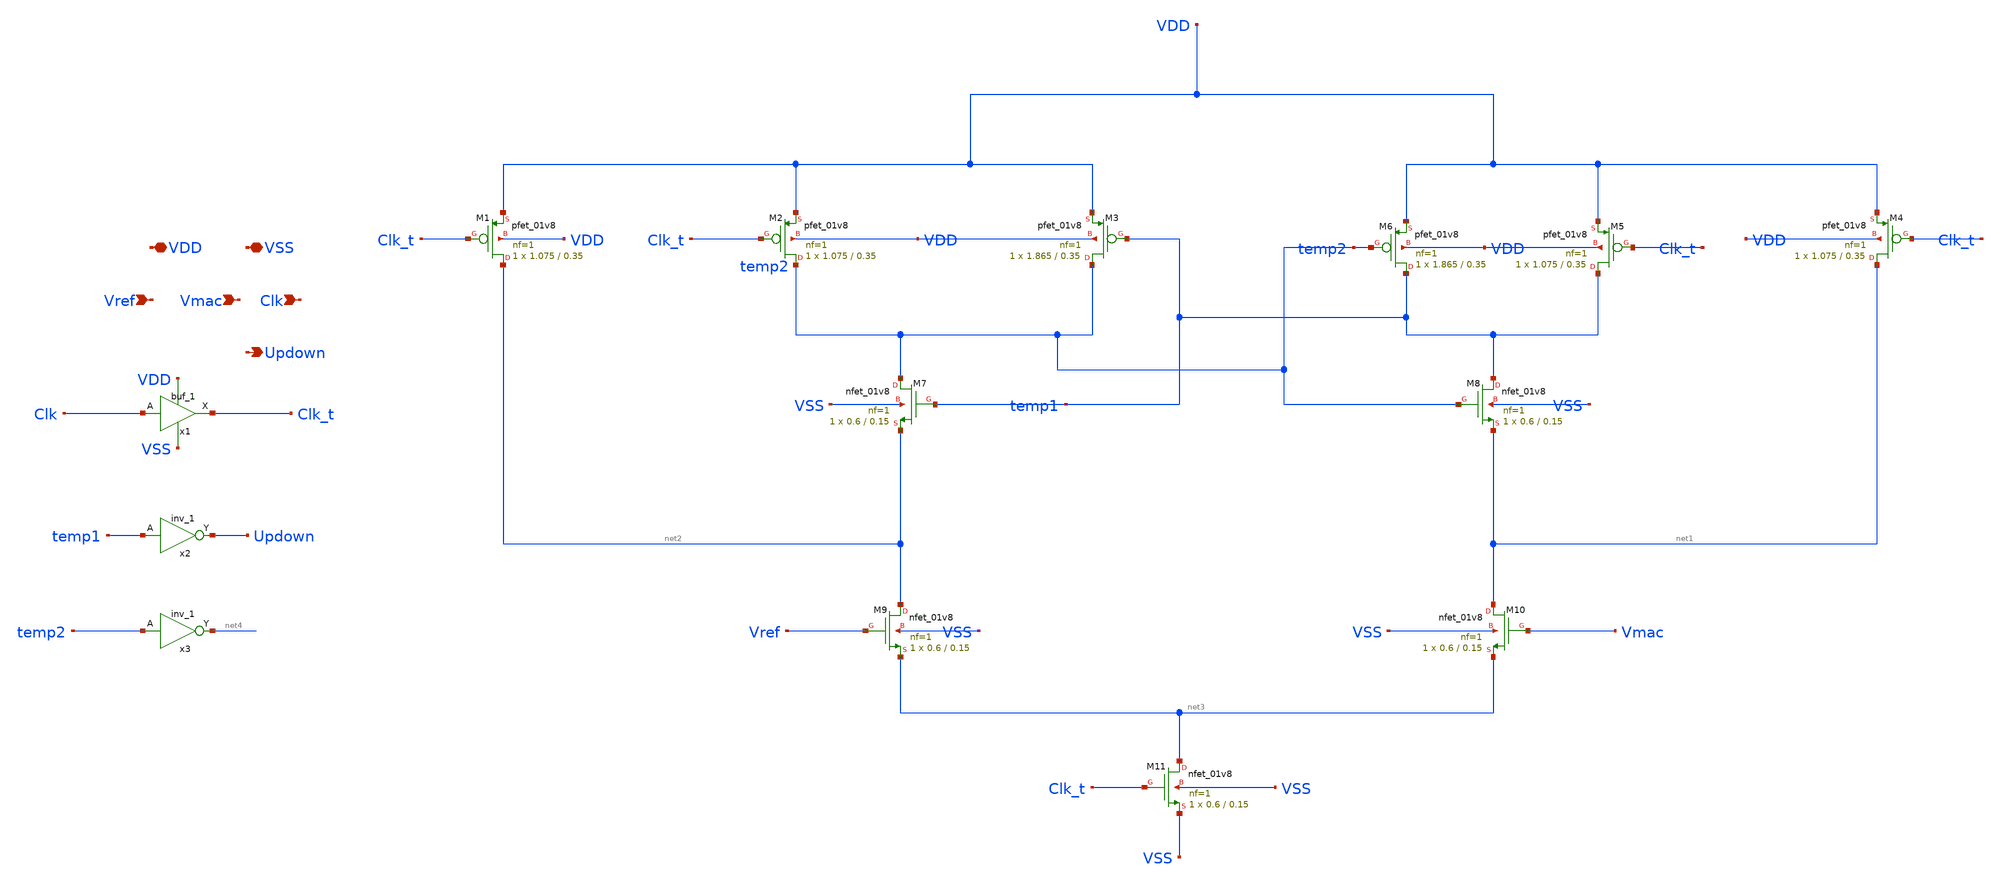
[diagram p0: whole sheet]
** sch_path: adc_comp/adc_8bit.sch
**.subckt adc_8bit VSS VDD Vref Vmac Clk Updown
*.iopin VSS
*.iopin VDD
*.ipin Vref
*.ipin Vmac
*.ipin Clk
*.opin Updown
x1 Clk VSS VNB VPB VDD Clk_t sky130_fd_sc_hd__buf_1
x2 temp1 VSS VNB VPB VDD Updown sky130_fd_sc_hd__inv_1
x3 temp2 VSS VNB VPB VDD net4 sky130_fd_sc_hd__inv_1
XM1 net2 Clk_t VDD VDD sky130_fd_pr__pfet_01v8 L=0.35 W=1.075 nf=1 ad='int((nf+1)/2) * W/nf * 0.29' as='int((nf+2)/2) * W/nf * 0.29'
+ pd='2*int((nf+1)/2) * (W/nf + 0.29)' ps='2*int((nf+2)/2) * (W/nf + 0.29)' nrd='0.29 / W' nrs='0.29 / W'
+ sa=0 sb=0 sd=0 mult=1 m=1
XM2 temp2 Clk_t VDD VDD sky130_fd_pr__pfet_01v8 L=0.35 W=1.075 nf=1 ad='int((nf+1)/2) * W/nf * 0.29'
+ as='int((nf+2)/2) * W/nf * 0.29' pd='2*int((nf+1)/2) * (W/nf + 0.29)' ps='2*int((nf+2)/2) * (W/nf + 0.29)'
+ nrd='0.29 / W' nrs='0.29 / W' sa=0 sb=0 sd=0 mult=1 m=1
XM3 temp2 temp1 VDD VDD sky130_fd_pr__pfet_01v8 L=0.35 W=1.865 nf=1 ad='int((nf+1)/2) * W/nf * 0.29'
+ as='int((nf+2)/2) * W/nf * 0.29' pd='2*int((nf+1)/2) * (W/nf + 0.29)' ps='2*int((nf+2)/2) * (W/nf + 0.29)'
+ nrd='0.29 / W' nrs='0.29 / W' sa=0 sb=0 sd=0 mult=1 m=1
XM4 net1 Clk_t VDD VDD sky130_fd_pr__pfet_01v8 L=0.35 W=1.075 nf=1 ad='int((nf+1)/2) * W/nf * 0.29' as='int((nf+2)/2) * W/nf * 0.29'
+ pd='2*int((nf+1)/2) * (W/nf + 0.29)' ps='2*int((nf+2)/2) * (W/nf + 0.29)' nrd='0.29 / W' nrs='0.29 / W'
+ sa=0 sb=0 sd=0 mult=1 m=1
XM5 temp1 Clk_t VDD VDD sky130_fd_pr__pfet_01v8 L=0.35 W=1.075 nf=1 ad='int((nf+1)/2) * W/nf * 0.29'
+ as='int((nf+2)/2) * W/nf * 0.29' pd='2*int((nf+1)/2) * (W/nf + 0.29)' ps='2*int((nf+2)/2) * (W/nf + 0.29)'
+ nrd='0.29 / W' nrs='0.29 / W' sa=0 sb=0 sd=0 mult=1 m=1
XM6 temp1 temp2 VDD VDD sky130_fd_pr__pfet_01v8 L=0.35 W=1.865 nf=1 ad='int((nf+1)/2) * W/nf * 0.29'
+ as='int((nf+2)/2) * W/nf * 0.29' pd='2*int((nf+1)/2) * (W/nf + 0.29)' ps='2*int((nf+2)/2) * (W/nf + 0.29)'
+ nrd='0.29 / W' nrs='0.29 / W' sa=0 sb=0 sd=0 mult=1 m=1
XM7 temp2 temp1 net2 VSS sky130_fd_pr__nfet_01v8 L=0.15 W=0.6 nf=1 ad='int((nf+1)/2) * W/nf * 0.29' as='int((nf+2)/2) * W/nf * 0.29'
+ pd='2*int((nf+1)/2) * (W/nf + 0.29)' ps='2*int((nf+2)/2) * (W/nf + 0.29)' nrd='0.29 / W' nrs='0.29 / W'
+ sa=0 sb=0 sd=0 mult=1 m=1
XM8 temp1 temp2 net1 VSS sky130_fd_pr__nfet_01v8 L=0.15 W=0.6 nf=1 ad='int((nf+1)/2) * W/nf * 0.29' as='int((nf+2)/2) * W/nf * 0.29'
+ pd='2*int((nf+1)/2) * (W/nf + 0.29)' ps='2*int((nf+2)/2) * (W/nf + 0.29)' nrd='0.29 / W' nrs='0.29 / W'
+ sa=0 sb=0 sd=0 mult=1 m=1
XM9 net2 Vref net3 VSS sky130_fd_pr__nfet_01v8 L=0.15 W=0.6 nf=1 ad='int((nf+1)/2) * W/nf * 0.29' as='int((nf+2)/2) * W/nf * 0.29'
+ pd='2*int((nf+1)/2) * (W/nf + 0.29)' ps='2*int((nf+2)/2) * (W/nf + 0.29)' nrd='0.29 / W' nrs='0.29 / W'
+ sa=0 sb=0 sd=0 mult=1 m=1
XM10 net1 Vmac net3 VSS sky130_fd_pr__nfet_01v8 L=0.15 W=0.6 nf=1 ad='int((nf+1)/2) * W/nf * 0.29' as='int((nf+2)/2) * W/nf * 0.29'
+ pd='2*int((nf+1)/2) * (W/nf + 0.29)' ps='2*int((nf+2)/2) * (W/nf + 0.29)' nrd='0.29 / W' nrs='0.29 / W'
+ sa=0 sb=0 sd=0 mult=1 m=1
XM11 net3 Clk_t VSS VSS sky130_fd_pr__nfet_01v8 L=0.15 W=0.6 nf=1 ad='int((nf+1)/2) * W/nf * 0.29' as='int((nf+2)/2) * W/nf * 0.29'
+ pd='2*int((nf+1)/2) * (W/nf + 0.29)' ps='2*int((nf+2)/2) * (W/nf + 0.29)' nrd='0.29 / W' nrs='0.29 / W'
+ sa=0 sb=0 sd=0 mult=1 m=1
**** begin user architecture code

** opencircuitdesign pdks install
.lib $::SKYWATER_MODELS/sky130.lib.spice tt
.include $::SKYWATER_STDCELLS/sky130_fd_sc_hd.spice

**** end user architecture code
**.ends
.end
